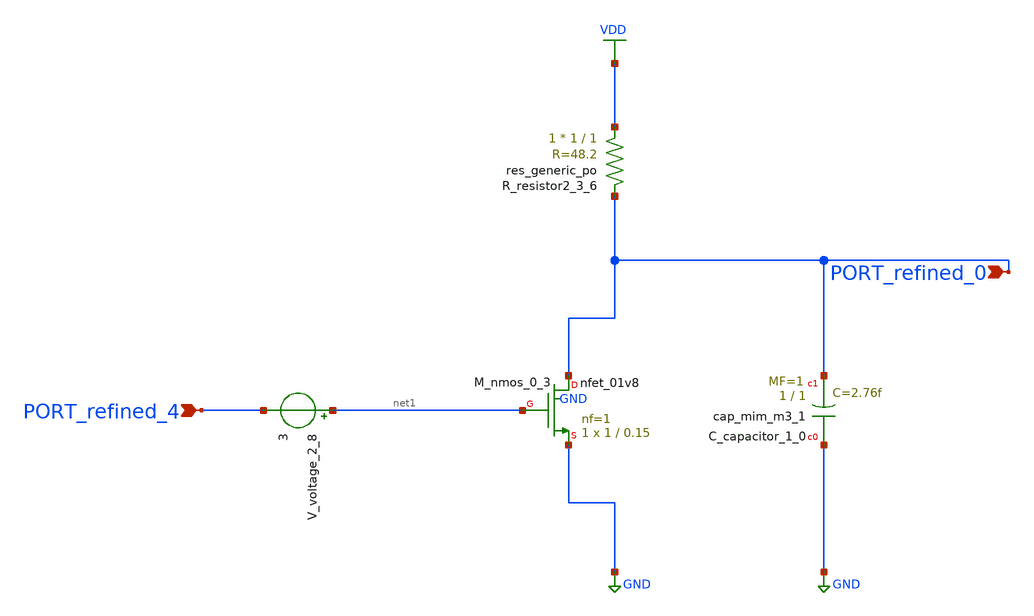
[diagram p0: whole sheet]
** sch_path: schematics/AMSNet/499.sch
**.subckt 499 PORT_refined_4 PORT_refined_0
*.ipin PORT_refined_4
*.ipin PORT_refined_0
XC_capacitor_1_0 GND PORT_refined_0 sky130_fd_pr__cap_mim_m3_1 W=1 L=1 MF=1 m=1
XM_nmos_0_3 PORT_refined_0 net1 GND GND sky130_fd_pr__nfet_01v8 L=0.15 W=1 nf=1 ad='int((1 + 1)/2) * 1 / 1 * 0.29'
+ as='int((1 + 2)/2) * 1 / 1 * 0.29' pd='2*int((1 + 1)/2) * (1 / 1 + 0.29)' ps='2*int((1 + 2)/2) * (1 / 1 + 0.29)'
+ nrd='0.29 / 1 ' nrs='0.29 / 1 ' sa=0 sb=0 sd=0 mult=1 m=1
XR_resistor2_3_6 VDD PORT_refined_0 sky130_fd_pr__res_generic_po W=1 L=1 m=1
V_voltage_2_8 net1 PORT_refined_4 3
**.ends
.GLOBAL GND
.GLOBAL VDD
.end
